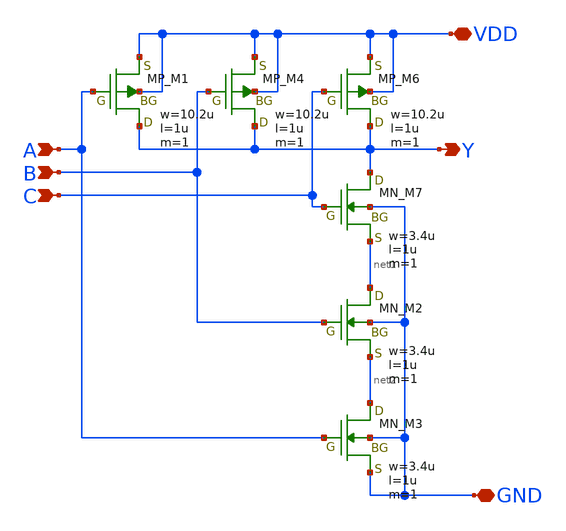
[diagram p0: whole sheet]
** sch_path: libs.tech/xschem/TR-1um_5_stdcell/NAND3.sch
**.subckt NAND3 B A Y GND VDD C
*.ipin B
*.ipin A
*.opin Y
*.iopin GND
*.iopin VDD
*.ipin C
XM1 Y A VDD VDD PMOS w=10.2u l=1u nrd=0 nrs=0 m=1
XM4 Y B VDD VDD PMOS w=10.2u l=1u nrd=0 nrs=0 m=1
XM6 Y C VDD VDD PMOS w=10.2u l=1u nrd=0 nrs=0 m=1
XM7 Y C net1 GND NMOS w=3.4u l=1u nrd=0 nrs=0 m=1
XM2 net1 B net2 GND NMOS w=3.4u l=1u nrd=0 nrs=0 m=1
XM3 net2 A GND GND NMOS w=3.4u l=1u nrd=0 nrs=0 m=1
**.ends
.end
